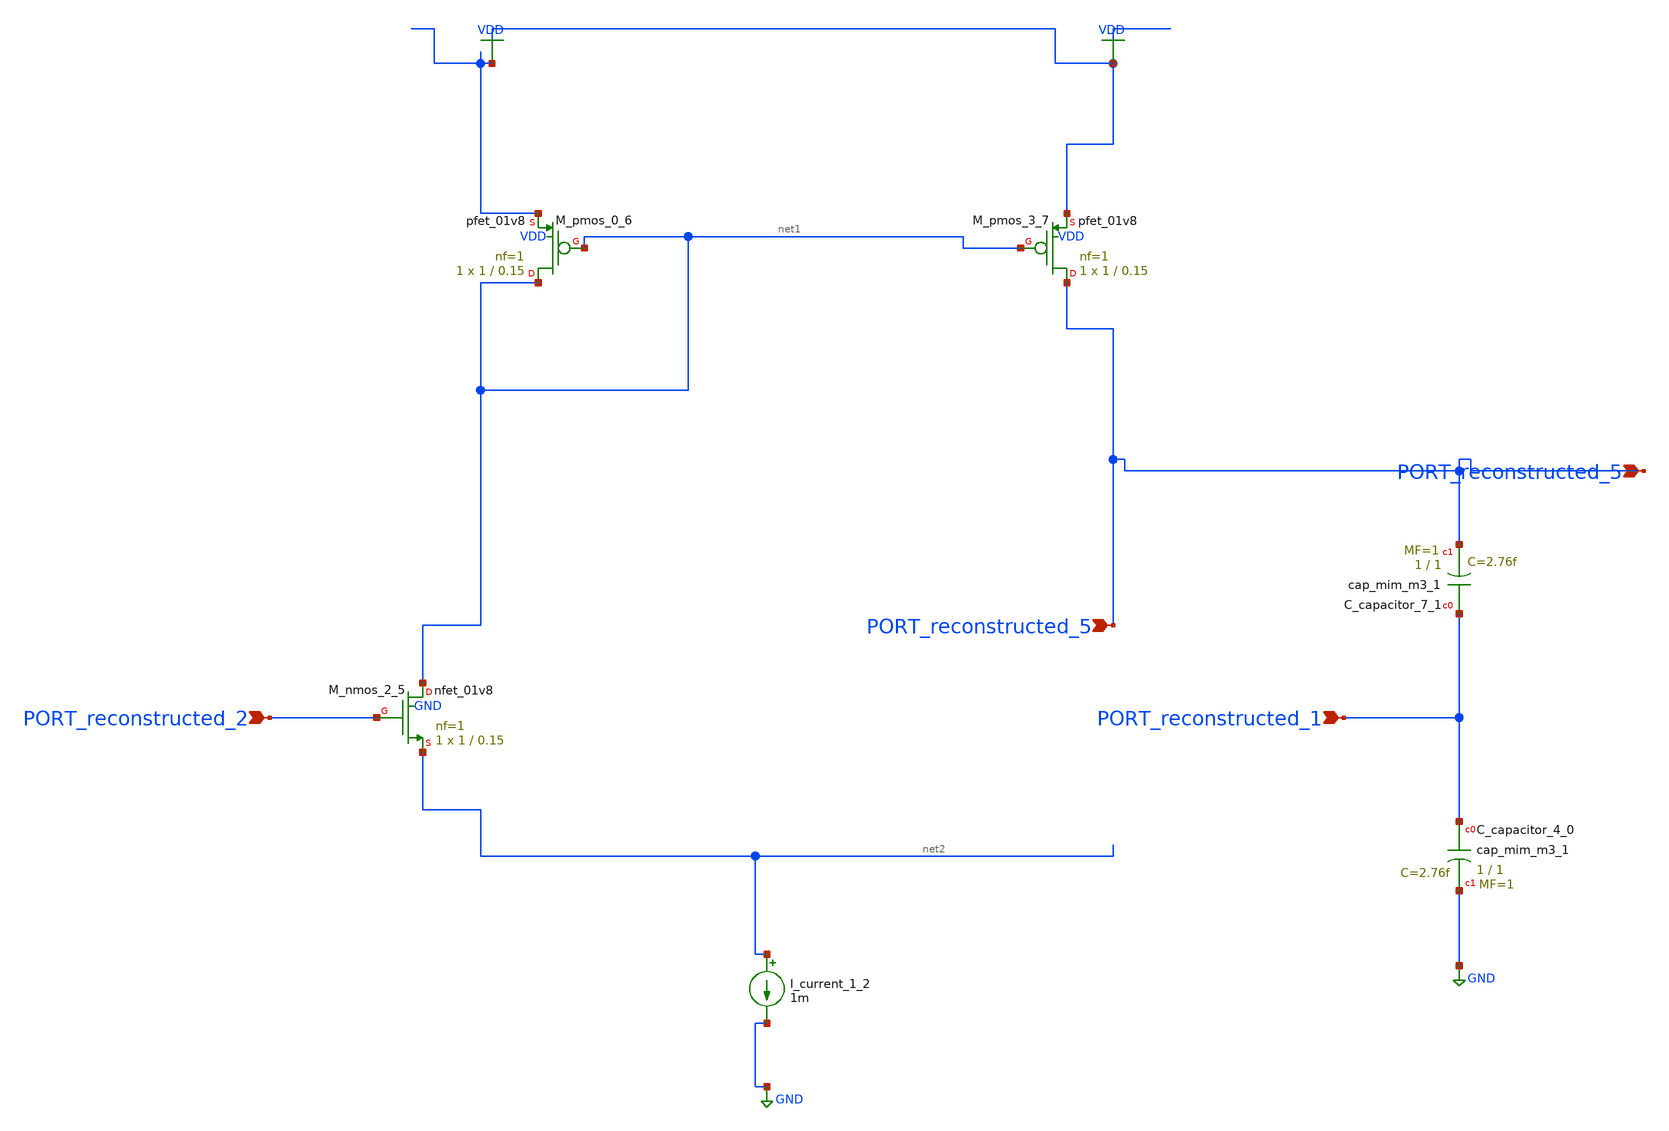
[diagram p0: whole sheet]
** sch_path: schematics/AMSNet/690.sch
**.subckt 690 PORT_reconstructed_1 PORT_reconstructed_5 PORT_reconstructed_5 PORT_reconstructed_2
*.ipin PORT_reconstructed_1
*.ipin PORT_reconstructed_5
*.ipin PORT_reconstructed_5
*.ipin PORT_reconstructed_2
XC_capacitor_4_0 PORT_reconstructed_1 GND sky130_fd_pr__cap_mim_m3_1 W=1 L=1 MF=1 m=1
XC_capacitor_7_1 PORT_reconstructed_1 PORT_reconstructed_5 sky130_fd_pr__cap_mim_m3_1 W=1 L=1 MF=1
+ m=1
I_current_1_2 net2 GND 1m
XM_nmos_2_5 net1 PORT_reconstructed_2 net2 GND sky130_fd_pr__nfet_01v8 L=0.15 W=1 nf=1 ad='int((1 + 1)/2) * 1 / 1 * 0.29'
+ as='int((1 + 2)/2) * 1 / 1 * 0.29' pd='2*int((1 + 1)/2) * (1 / 1 + 0.29)' ps='2*int((1 + 2)/2) * (1 / 1 + 0.29)'
+ nrd='0.29 / 1 ' nrs='0.29 / 1 ' sa=0 sb=0 sd=0 mult=1 m=1
XM_pmos_0_6 net1 net1 VDD VDD sky130_fd_pr__pfet_01v8 L=0.15 W=1 nf=1 ad='int((1 + 1)/2) * 1 / 1 * 0.29'
+ as='int((1 + 2)/2) * 1 / 1 * 0.29' pd='2*int((1 + 1)/2) * (1 / 1 + 0.29)' ps='2*int((1 + 2)/2) * (1 / 1 + 0.29)'
+ nrd='0.29 / 1 ' nrs='0.29 / 1 ' sa=0 sb=0 sd=0 mult=1 m=1
XM_pmos_3_7 PORT_reconstructed_5 net1 VDD VDD sky130_fd_pr__pfet_01v8 L=0.15 W=1 nf=1 ad='int((1 + 1)/2) * 1 / 1 * 0.29'
+ as='int((1 + 2)/2) * 1 / 1 * 0.29' pd='2*int((1 + 1)/2) * (1 / 1 + 0.29)' ps='2*int((1 + 2)/2) * (1 / 1 + 0.29)'
+ nrd='0.29 / 1 ' nrs='0.29 / 1 ' sa=0 sb=0 sd=0 mult=1 m=1
**.ends
.GLOBAL GND
.GLOBAL VDD
.end
